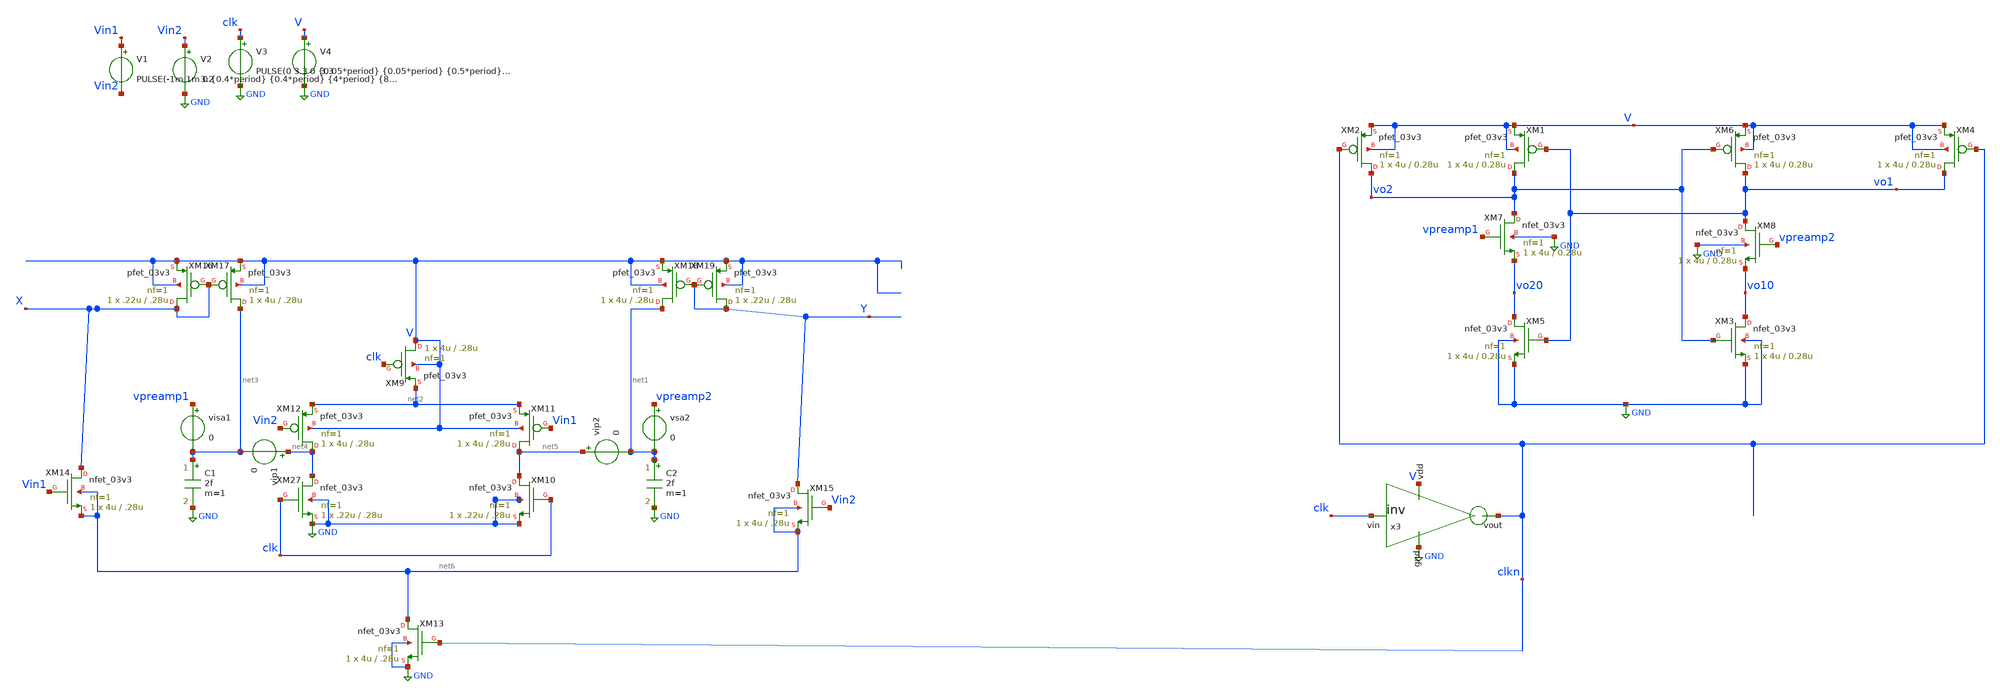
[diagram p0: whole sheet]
** sch_path: xschem/test/strongarm_tb/strongarm_DC_tb.sch
**.subckt strongarm_DC_tb
V3 clk GND PULSE(0 3.3 0 {0.05*period} {0.05*period} {0.5*period} {1*period})
V4 V GND 3.3
XM1 vo2 vo1 V V pfet_03v3 L=0.28u W=4u nf=1 ad='int((nf+1)/2) * W/nf * 0.18u' as='int((nf+2)/2) * W/nf * 0.18u'
+ pd='2*int((nf+1)/2) * (W/nf + 0.18u)' ps='2*int((nf+2)/2) * (W/nf + 0.18u)' nrd='0.18u / W' nrs='0.18u / W'
+ sa=0 sb=0 sd=0 m=1
XM2 vo2 clkn V V pfet_03v3 L=0.28u W=4u nf=1 ad='int((nf+1)/2) * W/nf * 0.18u' as='int((nf+2)/2) * W/nf * 0.18u'
+ pd='2*int((nf+1)/2) * (W/nf + 0.18u)' ps='2*int((nf+2)/2) * (W/nf + 0.18u)' nrd='0.18u / W' nrs='0.18u / W'
+ sa=0 sb=0 sd=0 m=1
XM3 vo10 vo2 GND GND nfet_03v3 L=0.28u W=4u nf=1 ad='int((nf+1)/2) * W/nf * 0.18u' as='int((nf+2)/2) * W/nf * 0.18u'
+ pd='2*int((nf+1)/2) * (W/nf + 0.18u)' ps='2*int((nf+2)/2) * (W/nf + 0.18u)' nrd='0.18u / W' nrs='0.18u / W'
+ sa=0 sb=0 sd=0 m=1
XM4 vo1 clkn V V pfet_03v3 L=0.28u W=4u nf=1 ad='int((nf+1)/2) * W/nf * 0.18u' as='int((nf+2)/2) * W/nf * 0.18u'
+ pd='2*int((nf+1)/2) * (W/nf + 0.18u)' ps='2*int((nf+2)/2) * (W/nf + 0.18u)' nrd='0.18u / W' nrs='0.18u / W'
+ sa=0 sb=0 sd=0 m=1
XM5 vo20 vo1 GND GND nfet_03v3 L=0.28u W=4u nf=1 ad='int((nf+1)/2) * W/nf * 0.18u' as='int((nf+2)/2) * W/nf * 0.18u'
+ pd='2*int((nf+1)/2) * (W/nf + 0.18u)' ps='2*int((nf+2)/2) * (W/nf + 0.18u)' nrd='0.18u / W' nrs='0.18u / W'
+ sa=0 sb=0 sd=0 m=1
XM6 vo1 vo2 V V pfet_03v3 L=0.28u W=4u nf=1 ad='int((nf+1)/2) * W/nf * 0.18u' as='int((nf+2)/2) * W/nf * 0.18u'
+ pd='2*int((nf+1)/2) * (W/nf + 0.18u)' ps='2*int((nf+2)/2) * (W/nf + 0.18u)' nrd='0.18u / W' nrs='0.18u / W'
+ sa=0 sb=0 sd=0 m=1
XM7 vo2 vpreamp1 vo20 GND nfet_03v3 L=0.28u W=4u nf=1 ad='int((nf+1)/2) * W/nf * 0.18u' as='int((nf+2)/2) * W/nf * 0.18u'
+ pd='2*int((nf+1)/2) * (W/nf + 0.18u)' ps='2*int((nf+2)/2) * (W/nf + 0.18u)' nrd='0.18u / W' nrs='0.18u / W'
+ sa=0 sb=0 sd=0 m=1
XM8 vo1 vpreamp2 vo10 GND nfet_03v3 L=0.28u W=4u nf=1 ad='int((nf+1)/2) * W/nf * 0.18u' as='int((nf+2)/2) * W/nf * 0.18u'
+ pd='2*int((nf+1)/2) * (W/nf + 0.18u)' ps='2*int((nf+2)/2) * (W/nf + 0.18u)' nrd='0.18u / W' nrs='0.18u / W'
+ sa=0 sb=0 sd=0 m=1
x3 V GND clkn clk inv cl=0.28u wp=0.44u wn=0.22u wx=.22u mx=1
XM27 net4 clk GND GND nfet_03v3 L=.28u W=.22u nf=1 ad='int((nf+1)/2) * W/nf * 0.18u' as='int((nf+2)/2) * W/nf * 0.18u'
+ pd='2*int((nf+1)/2) * (W/nf + 0.18u)' ps='2*int((nf+2)/2) * (W/nf + 0.18u)' nrd='0.18u / W' nrs='0.18u / W'
+ sa=0 sb=0 sd=0 m=1
XM9 V clk net2 V pfet_03v3 L=.28u W=4u nf=1 ad='int((nf+1)/2) * W/nf * 0.18u' as='int((nf+2)/2) * W/nf * 0.18u'
+ pd='2*int((nf+1)/2) * (W/nf + 0.18u)' ps='2*int((nf+2)/2) * (W/nf + 0.18u)' nrd='0.18u / W' nrs='0.18u / W'
+ sa=0 sb=0 sd=0 m=1
XM11 net5 Vin1 net2 V pfet_03v3 L=.28u W=4u nf=1 ad='int((nf+1)/2) * W/nf * 0.18u' as='int((nf+2)/2) * W/nf * 0.18u'
+ pd='2*int((nf+1)/2) * (W/nf + 0.18u)' ps='2*int((nf+2)/2) * (W/nf + 0.18u)' nrd='0.18u / W' nrs='0.18u / W'
+ sa=0 sb=0 sd=0 m=1
XM12 net4 Vin2 net2 V pfet_03v3 L=.28u W=4u nf=1 ad='int((nf+1)/2) * W/nf * 0.18u' as='int((nf+2)/2) * W/nf * 0.18u'
+ pd='2*int((nf+1)/2) * (W/nf + 0.18u)' ps='2*int((nf+2)/2) * (W/nf + 0.18u)' nrd='0.18u / W' nrs='0.18u / W'
+ sa=0 sb=0 sd=0 m=1
C1 net3 GND 2f m=1
C2 net1 GND 2f m=1
V1 Vin1 Vin2 PULSE(-1m 1m 0 {0.4*period} {0.4*period} {4*period} {8*period})
V2 Vin2 GND 3.2
vip1 net4 net3 0
visa1 vpreamp1 net3 0
vip2 net5 net1 0
vsa2 vpreamp2 net1 0
XM10 net5 clk GND GND nfet_03v3 L=.28u W=.22u nf=1 ad='int((nf+1)/2) * W/nf * 0.18u' as='int((nf+2)/2) * W/nf * 0.18u'
+ pd='2*int((nf+1)/2) * (W/nf + 0.18u)' ps='2*int((nf+2)/2) * (W/nf + 0.18u)' nrd='0.18u / W' nrs='0.18u / W'
+ sa=0 sb=0 sd=0 m=1
XM13 net6 clkn GND GND nfet_03v3 L=.28u W=4u nf=1 ad='int((nf+1)/2) * W/nf * 0.18u' as='int((nf+2)/2) * W/nf * 0.18u'
+ pd='2*int((nf+1)/2) * (W/nf + 0.18u)' ps='2*int((nf+2)/2) * (W/nf + 0.18u)' nrd='0.18u / W' nrs='0.18u / W'
+ sa=0 sb=0 sd=0 m=1
XM14 X Vin1 net6 net6 nfet_03v3 L=.28u W=4u nf=1 ad='int((nf+1)/2) * W/nf * 0.18u' as='int((nf+2)/2) * W/nf * 0.18u'
+ pd='2*int((nf+1)/2) * (W/nf + 0.18u)' ps='2*int((nf+2)/2) * (W/nf + 0.18u)' nrd='0.18u / W' nrs='0.18u / W'
+ sa=0 sb=0 sd=0 m=1
XM15 Y Vin2 net6 net6 nfet_03v3 L=.28u W=4u nf=1 ad='int((nf+1)/2) * W/nf * 0.18u' as='int((nf+2)/2) * W/nf * 0.18u'
+ pd='2*int((nf+1)/2) * (W/nf + 0.18u)' ps='2*int((nf+2)/2) * (W/nf + 0.18u)' nrd='0.18u / W' nrs='0.18u / W'
+ sa=0 sb=0 sd=0 m=1
XM16 X X V V pfet_03v3 L=.28u W=.22u nf=1 ad='int((nf+1)/2) * W/nf * 0.18u' as='int((nf+2)/2) * W/nf * 0.18u'
+ pd='2*int((nf+1)/2) * (W/nf + 0.18u)' ps='2*int((nf+2)/2) * (W/nf + 0.18u)' nrd='0.18u / W' nrs='0.18u / W'
+ sa=0 sb=0 sd=0 m=1
XM17 net3 X V V pfet_03v3 L=.28u W=4u nf=1 ad='int((nf+1)/2) * W/nf * 0.18u' as='int((nf+2)/2) * W/nf * 0.18u'
+ pd='2*int((nf+1)/2) * (W/nf + 0.18u)' ps='2*int((nf+2)/2) * (W/nf + 0.18u)' nrd='0.18u / W' nrs='0.18u / W'
+ sa=0 sb=0 sd=0 m=1
XM18 net1 Y V V pfet_03v3 L=.28u W=4u nf=1 ad='int((nf+1)/2) * W/nf * 0.18u' as='int((nf+2)/2) * W/nf * 0.18u'
+ pd='2*int((nf+1)/2) * (W/nf + 0.18u)' ps='2*int((nf+2)/2) * (W/nf + 0.18u)' nrd='0.18u / W' nrs='0.18u / W'
+ sa=0 sb=0 sd=0 m=1
XM19 Y Y V V pfet_03v3 L=.28u W=.22u nf=1 ad='int((nf+1)/2) * W/nf * 0.18u' as='int((nf+2)/2) * W/nf * 0.18u'
+ pd='2*int((nf+1)/2) * (W/nf + 0.18u)' ps='2*int((nf+2)/2) * (W/nf + 0.18u)' nrd='0.18u / W' nrs='0.18u / W'
+ sa=0 sb=0 sd=0 m=1
**** begin user architecture code



.param period=50n
.param stoptime={100*period}
.tran {0.01*stoptime} {stoptime} uic
.control
save all
run
*plot {(vin1-vin2)/abs(vin1-vin2)} {(vo1-vo2)} clk
*plot {(vin1-vin2)/abs(vin1-vin2)} {(vpreamp1-vpreamp2)} clk
*plot {vo11-vo1} {vo22-vo2} clk
*plot vo10 vo20
*plot vpreamp1 vo1 sareset
plot {vo2-vo1} {1000*(vin1-vin2)} clk
plot vo1 vo2 clk
*plot {(vin1-vin2)*10} {(vpreamp1-vpreamp2)} {clk /330} {vin2/(100)}
plot {(vin1-vin2)*1000} vpreamp1 vpreamp2 {clk} {vin2}
plot {(vpreamp1-vpreamp2)} {(vin1-vin2)} {clk/330}
plot X Y clk
plot {(X-Y)} {clk/3000}
*plot clk sareset
*plot i(vip1) i(vip2) i(visa1) i(vsa2) clk/3300
.endc


.include $env(PDK_ROOT)/$env(PDK)/libs.tech/ngspice/design.ngspice
.lib $env(PDK_ROOT)/$env(PDK)/libs.tech/ngspice/sm141064.ngspice typical

**** end user architecture code
**.ends

* expanding   symbol:  inv.sym # of pins=4
** sym_path: xschem/designs/inv.sym
** sch_path: xschem/designs/inv.sch
.subckt inv vdd gnd vout vin  cl=0.28u wp=0.44u wn=0.22u wx=0.22u mx=1
*.ipin gnd
*.ipin vdd
*.ipin vin
*.opin vout
XM1 gnd vin vout gnd nfet_03v3 L=0.28u W=Wx nf=1 ad='int((nf+1)/2) * W/nf * 0.18u' as='int((nf+2)/2) * W/nf * 0.18u'
+ pd='2*int((nf+1)/2) * (W/nf + 0.18u)' ps='2*int((nf+2)/2) * (W/nf + 0.18u)' nrd='0.18u / W' nrs='0.18u / W'
+ sa=0 sb=0 sd=0 m=1
XM2 vdd vin vout vdd pfet_03v3 L=0.28u W=Wx nf=1 ad='int((nf+1)/2) * W/nf * 0.18u' as='int((nf+2)/2) * W/nf * 0.18u'
+ pd='2*int((nf+1)/2) * (W/nf + 0.18u)' ps='2*int((nf+2)/2) * (W/nf + 0.18u)' nrd='0.18u / W' nrs='0.18u / W'
+ sa=0 sb=0 sd=0 m=1
.ends

.GLOBAL GND
.end
